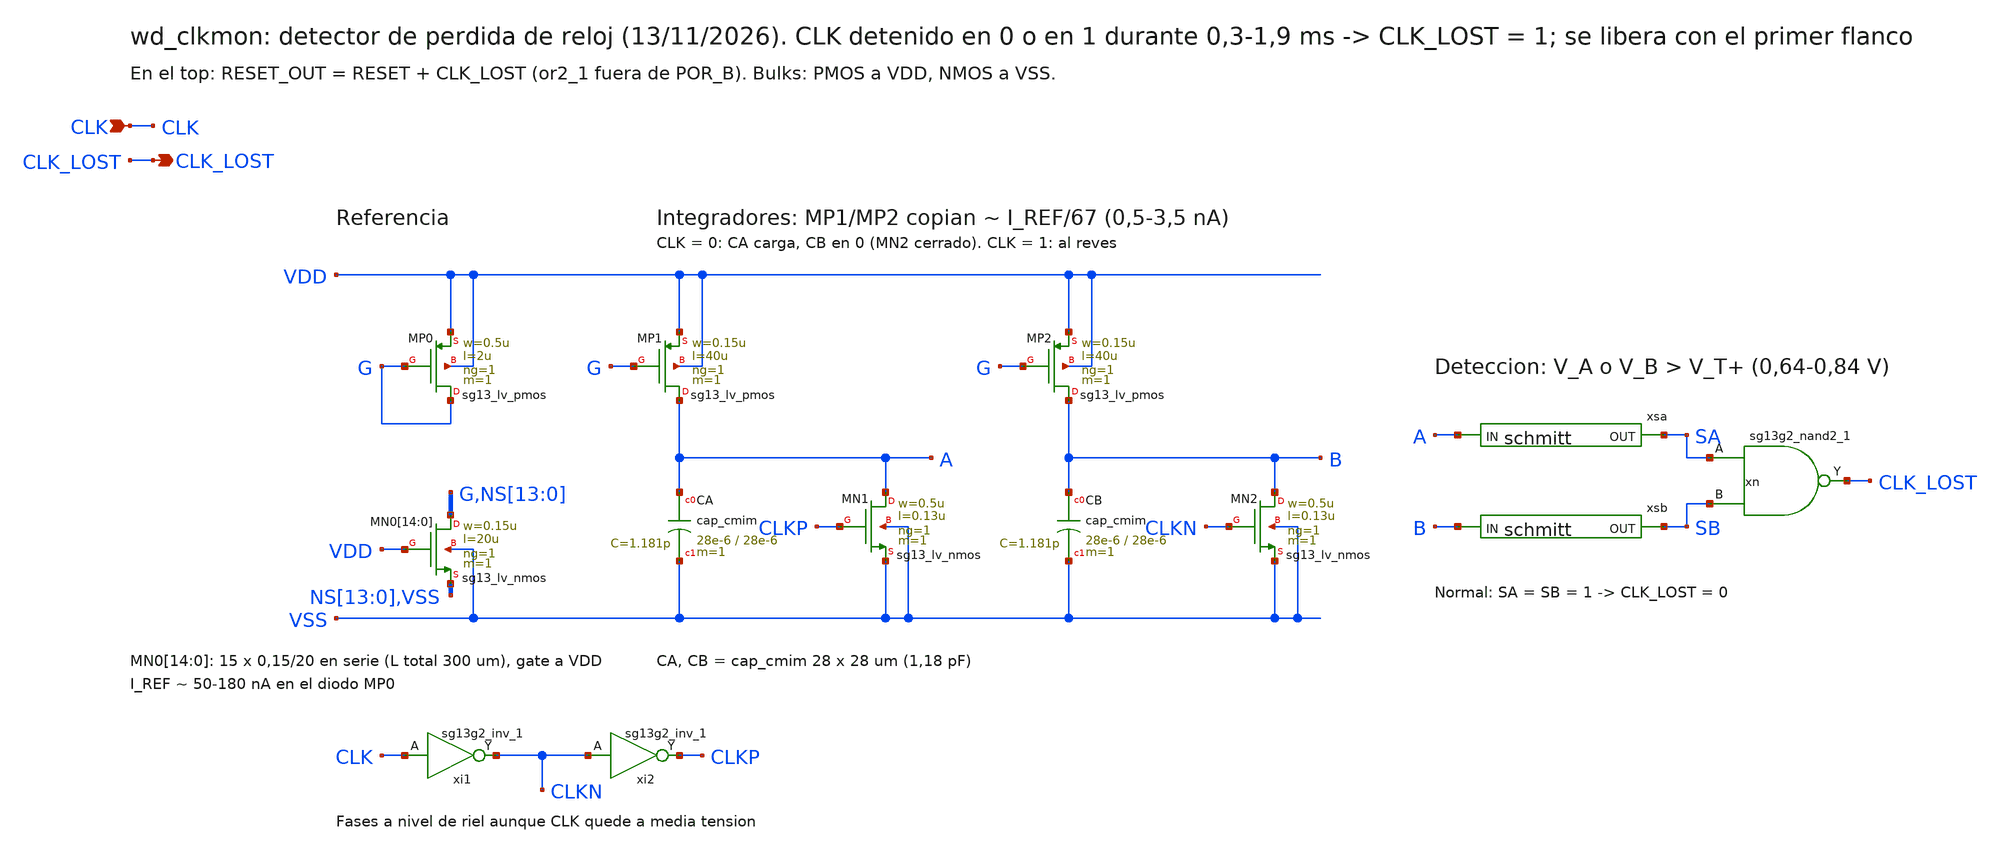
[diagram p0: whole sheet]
** sch_path: design/blocks/clkmon/schematic/wd_clkmon.sch
**.subckt wd_clkmon CLK CLK_LOST
*.ipin CLK
*.opin CLK_LOST
XMP0 G G VDD VDD sg13_lv_pmos w=0.5u l=2u ng=1 m=1 mm_ok=1
XMN0[14] G VDD NS[13] VSS sg13_lv_nmos w=0.15u l=20u ng=1 m=1 mm_ok=1
XMN0[13] NS[13] VDD NS[12] VSS sg13_lv_nmos w=0.15u l=20u ng=1 m=1 mm_ok=1
XMN0[12] NS[12] VDD NS[11] VSS sg13_lv_nmos w=0.15u l=20u ng=1 m=1 mm_ok=1
XMN0[11] NS[11] VDD NS[10] VSS sg13_lv_nmos w=0.15u l=20u ng=1 m=1 mm_ok=1
XMN0[10] NS[10] VDD NS[9] VSS sg13_lv_nmos w=0.15u l=20u ng=1 m=1 mm_ok=1
XMN0[9] NS[9] VDD NS[8] VSS sg13_lv_nmos w=0.15u l=20u ng=1 m=1 mm_ok=1
XMN0[8] NS[8] VDD NS[7] VSS sg13_lv_nmos w=0.15u l=20u ng=1 m=1 mm_ok=1
XMN0[7] NS[7] VDD NS[6] VSS sg13_lv_nmos w=0.15u l=20u ng=1 m=1 mm_ok=1
XMN0[6] NS[6] VDD NS[5] VSS sg13_lv_nmos w=0.15u l=20u ng=1 m=1 mm_ok=1
XMN0[5] NS[5] VDD NS[4] VSS sg13_lv_nmos w=0.15u l=20u ng=1 m=1 mm_ok=1
XMN0[4] NS[4] VDD NS[3] VSS sg13_lv_nmos w=0.15u l=20u ng=1 m=1 mm_ok=1
XMN0[3] NS[3] VDD NS[2] VSS sg13_lv_nmos w=0.15u l=20u ng=1 m=1 mm_ok=1
XMN0[2] NS[2] VDD NS[1] VSS sg13_lv_nmos w=0.15u l=20u ng=1 m=1 mm_ok=1
XMN0[1] NS[1] VDD NS[0] VSS sg13_lv_nmos w=0.15u l=20u ng=1 m=1 mm_ok=1
XMN0[0] NS[0] VDD VSS VSS sg13_lv_nmos w=0.15u l=20u ng=1 m=1 mm_ok=1
XMP1 A G VDD VDD sg13_lv_pmos w=0.15u l=40u ng=1 m=1 mm_ok=1
XCA A VSS cap_cmim w=28e-6 l=28e-6 m=1 mm_ok=1
XMN1 A CLKP VSS VSS sg13_lv_nmos w=0.5u l=0.13u ng=1 m=1 mm_ok=1
XMP2 B G VDD VDD sg13_lv_pmos w=0.15u l=40u ng=1 m=1 mm_ok=1
XCB B VSS cap_cmim w=28e-6 l=28e-6 m=1 mm_ok=1
XMN2 B CLKN VSS VSS sg13_lv_nmos w=0.5u l=0.13u ng=1 m=1 mm_ok=1
xi1 CLKN CLK VDD VSS sg13g2_inv_1
xi2 CLKP CLKN VDD VSS sg13g2_inv_1
xsa A SA VDD VSS schmitt
xsb B SB VDD VSS schmitt
xn CLK_LOST SA SB VDD VSS sg13g2_nand2_1
**.ends

* expanding   symbol:  sg13g2_inv_1.sym # of pins=2
** sym_path: sg13g2_inv_1.sym
** sch_path: sg13g2_inv_1.sch
.subckt sg13g2_inv_1 Y A VDD VSS
*.opin Y
*.ipin A
*.iopin VDD
*.iopin VSS
XM1 Y A VSS VSS sg13_lv_nmos w=740.00n l=130.00n ng=1 m=1 mm_ok=1
XM2 Y A VDD VDD sg13_lv_pmos w=1.12u l=130.00n ng=1 m=1 mm_ok=1
.ends


* expanding   symbol:  schmitt.sym # of pins=2
** sym_path: design/blocks/schmitt/schematic/schmitt.sym
** sch_path: design/blocks/schmitt/schematic/schmitt.sch
.subckt schmitt IN OUT VDD VSS
*.opin OUT
*.ipin IN
XM4 net1 IN VDD VDD sg13_lv_pmos w=1.04u l=0.13u ng=1 m=1 mm_ok=1
XM6 OUT IN net2 VSS sg13_lv_nmos w=0.76u l=0.13u ng=1 m=1 mm_ok=1
XM5 OUT IN net1 VDD sg13_lv_pmos w=1.04u l=0.13u ng=1 m=1 mm_ok=1
XM7 net2 IN VSS VSS sg13_lv_nmos w=0.76u l=0.13u ng=1 m=1 mm_ok=1
XM8 VSS OUT net1 VDD sg13_lv_pmos w=0.42u l=0.13u ng=1 m=1 mm_ok=1
XM9 VDD OUT net2 VSS sg13_lv_nmos w=0.42u l=0.13u ng=1 m=1 mm_ok=1
.ends


* expanding   symbol:  sg13g2_nand2_1.sym # of pins=3
** sym_path: sg13g2_nand2_1.sym
** sch_path: sg13g2_nand2_1.sch
.subckt sg13g2_nand2_1 Y A B VDD VSS
*.iopin VDD
*.iopin VSS
*.ipin A
*.ipin B
*.opin Y
XM1 Y A net1 VSS sg13_lv_nmos w=740.00n l=130.00n ng=1 m=1 mm_ok=1
XM2 net1 B VSS VSS sg13_lv_nmos w=740.00n l=130.00n ng=1 m=1 mm_ok=1
XM3 Y A VDD VDD sg13_lv_pmos w=1.12u l=130.00n ng=1 m=1 mm_ok=1
XM4 Y B VDD VDD sg13_lv_pmos w=1.12u l=130.00n ng=1 m=1 mm_ok=1
.ends

.end
